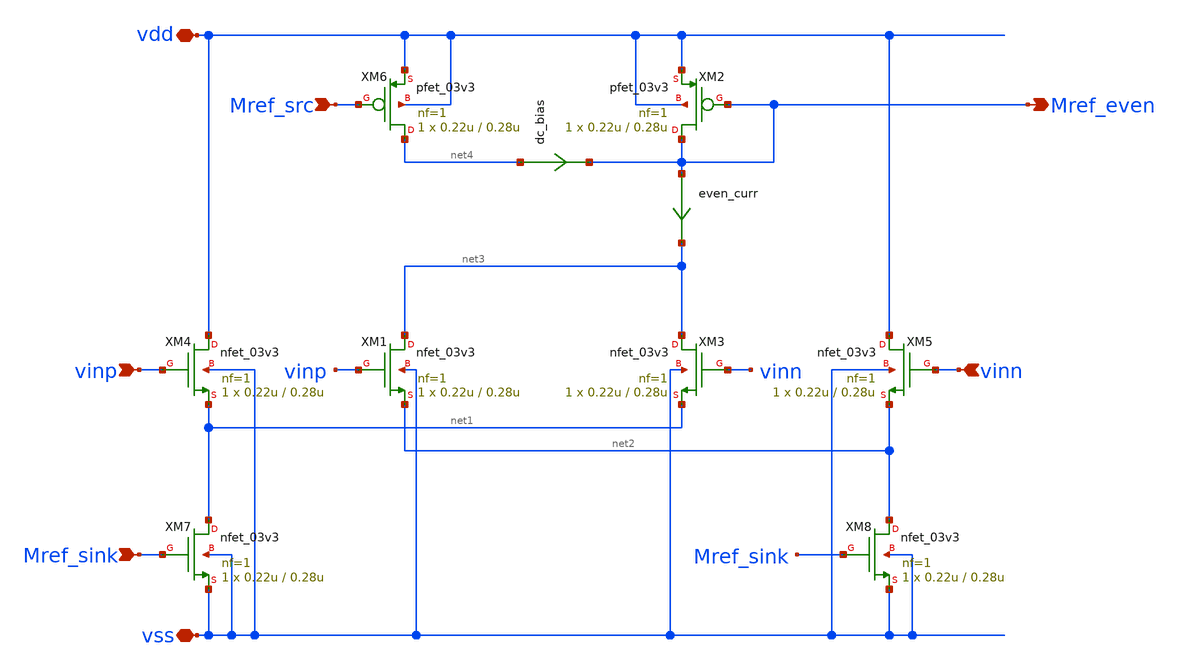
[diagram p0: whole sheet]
** sch_path: designs/libs/core_analog/quad_diff_in/quad_diff_in.sch
**.subckt quad_diff_in vdd vss vinp vinn Mref_src Mref_sink Mref_even
*.iopin vdd
*.iopin vss
*.ipin vinp
*.ipin vinn
*.ipin Mref_src
*.ipin Mref_sink
*.opin Mref_even
XM1 net3 vinp net2 vss nfet_03v3 L=0.28u W=0.22u nf=1 ad='int((nf+1)/2) * W/nf * 0.18u' as='int((nf+2)/2) * W/nf * 0.18u'
+ pd='2*int((nf+1)/2) * (W/nf + 0.18u)' ps='2*int((nf+2)/2) * (W/nf + 0.18u)' nrd='0.18u / W' nrs='0.18u / W'
+ sa=0 sb=0 sd=0 m=1
XM2 Mref_even Mref_even vdd vdd pfet_03v3 L=0.28u W=0.22u nf=1 ad='int((nf+1)/2) * W/nf * 0.18u' as='int((nf+2)/2) * W/nf * 0.18u'
+ pd='2*int((nf+1)/2) * (W/nf + 0.18u)' ps='2*int((nf+2)/2) * (W/nf + 0.18u)' nrd='0.18u / W' nrs='0.18u / W'
+ sa=0 sb=0 sd=0 m=1
XM3 net3 vinn net1 vss nfet_03v3 L=0.28u W=0.22u nf=1 ad='int((nf+1)/2) * W/nf * 0.18u' as='int((nf+2)/2) * W/nf * 0.18u'
+ pd='2*int((nf+1)/2) * (W/nf + 0.18u)' ps='2*int((nf+2)/2) * (W/nf + 0.18u)' nrd='0.18u / W' nrs='0.18u / W'
+ sa=0 sb=0 sd=0 m=1
XM4 vdd vinp net1 vss nfet_03v3 L=0.28u W=0.22u nf=1 ad='int((nf+1)/2) * W/nf * 0.18u' as='int((nf+2)/2) * W/nf * 0.18u'
+ pd='2*int((nf+1)/2) * (W/nf + 0.18u)' ps='2*int((nf+2)/2) * (W/nf + 0.18u)' nrd='0.18u / W' nrs='0.18u / W'
+ sa=0 sb=0 sd=0 m=1
XM5 vdd vinn net2 vss nfet_03v3 L=0.28u W=0.22u nf=1 ad='int((nf+1)/2) * W/nf * 0.18u' as='int((nf+2)/2) * W/nf * 0.18u'
+ pd='2*int((nf+1)/2) * (W/nf + 0.18u)' ps='2*int((nf+2)/2) * (W/nf + 0.18u)' nrd='0.18u / W' nrs='0.18u / W'
+ sa=0 sb=0 sd=0 m=1
even_curr Mref_even net3 0
.save i(even_curr)
XM6 net4 Mref_src vdd vdd pfet_03v3 L=0.28u W=0.22u nf=1 ad='int((nf+1)/2) * W/nf * 0.18u' as='int((nf+2)/2) * W/nf * 0.18u'
+ pd='2*int((nf+1)/2) * (W/nf + 0.18u)' ps='2*int((nf+2)/2) * (W/nf + 0.18u)' nrd='0.18u / W' nrs='0.18u / W'
+ sa=0 sb=0 sd=0 m=1
dc_bias net4 Mref_even 0
.save i(dc_bias)
XM7 net1 Mref_sink vss vss nfet_03v3 L=0.28u W=0.22u nf=1 ad='int((nf+1)/2) * W/nf * 0.18u' as='int((nf+2)/2) * W/nf * 0.18u'
+ pd='2*int((nf+1)/2) * (W/nf + 0.18u)' ps='2*int((nf+2)/2) * (W/nf + 0.18u)' nrd='0.18u / W' nrs='0.18u / W'
+ sa=0 sb=0 sd=0 m=1
XM8 net2 Mref_sink vss vss nfet_03v3 L=0.28u W=0.22u nf=1 ad='int((nf+1)/2) * W/nf * 0.18u' as='int((nf+2)/2) * W/nf * 0.18u'
+ pd='2*int((nf+1)/2) * (W/nf + 0.18u)' ps='2*int((nf+2)/2) * (W/nf + 0.18u)' nrd='0.18u / W' nrs='0.18u / W'
+ sa=0 sb=0 sd=0 m=1
**.ends
.end
